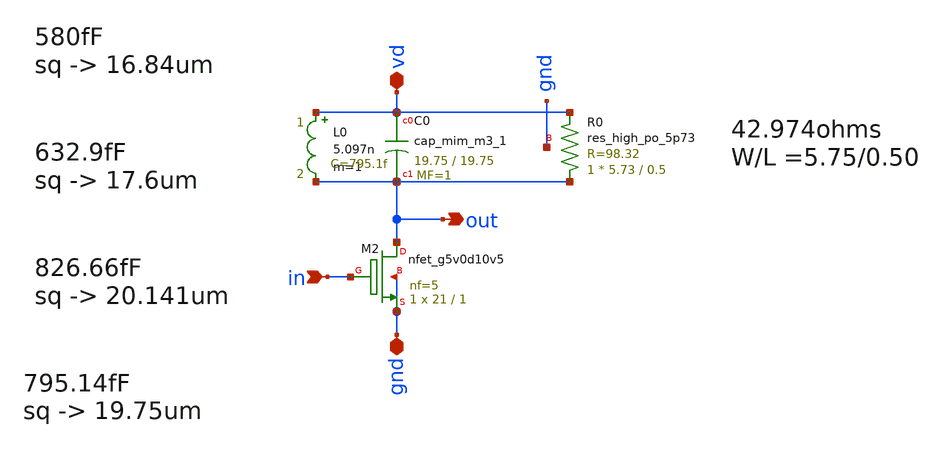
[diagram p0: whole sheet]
** sch_path: ask_modulator/xschem/ask-modulator.sch
**.subckt ask-modulator gnd in out vd
*.iopin gnd
*.ipin in
*.opin out
*.iopin vd
XM2 out in gnd gnd sky130_fd_pr__nfet_g5v0d10v5 L=1 W=21 nf=5 ad='int((nf+1)/2) * W/nf * 0.29' as='int((nf+2)/2) * W/nf * 0.29'
+ pd='2*int((nf+1)/2) * (W/nf + 0.29)' ps='2*int((nf+2)/2) * (W/nf + 0.29)' nrd='0.29 / W' nrs='0.29 / W'
+ sa=0 sb=0 sd=0 mult=1 m=1
L0 vd out 5.097n m=1
XC0 vd out sky130_fd_pr__cap_mim_m3_1 W=19.75 L=19.75 MF=1 m=1
XR0 out vd gnd sky130_fd_pr__res_high_po_5p73 L=0.5 mult=1 m=1
**.ends
.end
